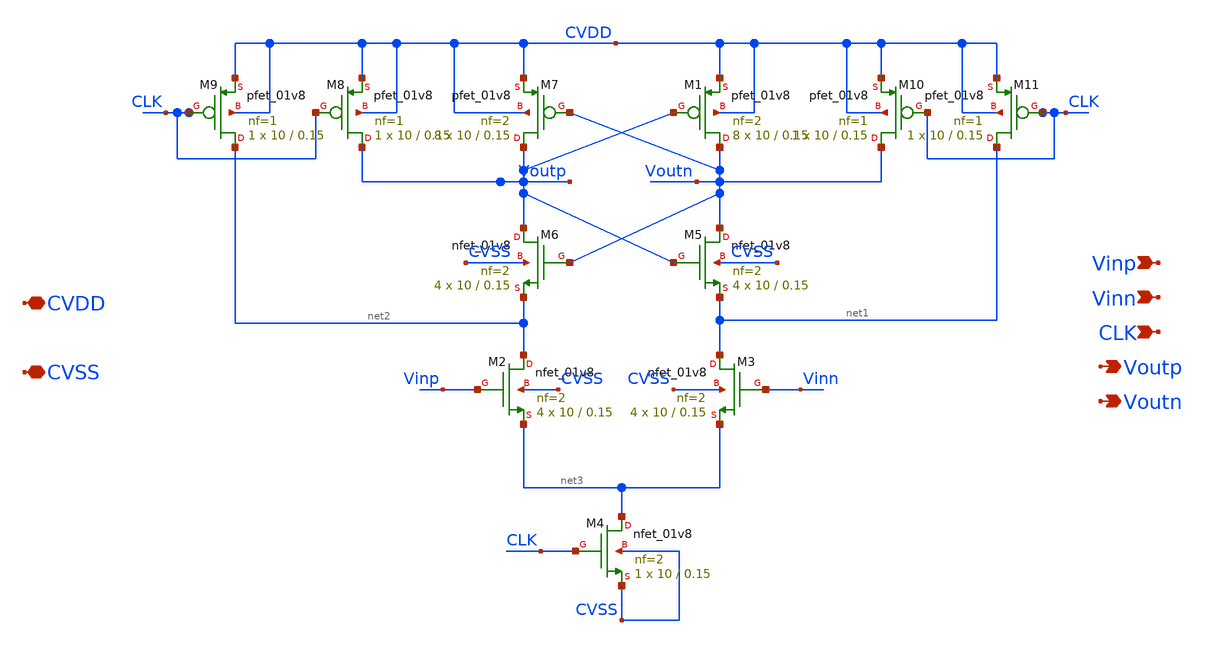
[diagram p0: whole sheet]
** sch_path: xschem/Comparator.sch
**.subckt Comparator CVDD CVSS Vinp Vinn CLK Voutp Voutn
*.iopin CVDD
*.iopin CVSS
*.ipin Vinp
*.ipin Vinn
*.ipin CLK
*.opin Voutp
*.opin Voutn
XM1 Voutn Voutp CVDD CVDD sky130_fd_pr__pfet_01v8 L=0.15 W=10 nf=2 ad='int((nf+1)/2) * W/nf * 0.29' as='int((nf+2)/2) * W/nf * 0.29'
+ pd='2*int((nf+1)/2) * (W/nf + 0.29)' ps='2*int((nf+2)/2) * (W/nf + 0.29)' nrd='0.29 / W' nrs='0.29 / W'
+ sa=0 sb=0 sd=0 mult=8 m=8
XM2 net2 Vinp net3 CVSS sky130_fd_pr__nfet_01v8 L=0.15 W=10 nf=2 ad='int((nf+1)/2) * W/nf * 0.29' as='int((nf+2)/2) * W/nf * 0.29'
+ pd='2*int((nf+1)/2) * (W/nf + 0.29)' ps='2*int((nf+2)/2) * (W/nf + 0.29)' nrd='0.29 / W' nrs='0.29 / W'
+ sa=0 sb=0 sd=0 mult=4 m=4
XM3 net1 Vinn net3 CVSS sky130_fd_pr__nfet_01v8 L=0.15 W=10 nf=2 ad='int((nf+1)/2) * W/nf * 0.29' as='int((nf+2)/2) * W/nf * 0.29'
+ pd='2*int((nf+1)/2) * (W/nf + 0.29)' ps='2*int((nf+2)/2) * (W/nf + 0.29)' nrd='0.29 / W' nrs='0.29 / W'
+ sa=0 sb=0 sd=0 mult=4 m=4
XM4 net3 CLK CVSS CVSS sky130_fd_pr__nfet_01v8 L=0.15 W=10 nf=2 ad='int((nf+1)/2) * W/nf * 0.29' as='int((nf+2)/2) * W/nf * 0.29'
+ pd='2*int((nf+1)/2) * (W/nf + 0.29)' ps='2*int((nf+2)/2) * (W/nf + 0.29)' nrd='0.29 / W' nrs='0.29 / W'
+ sa=0 sb=0 sd=0 mult=1 m=1
XM5 Voutn Voutp net1 CVSS sky130_fd_pr__nfet_01v8 L=0.15 W=10 nf=2 ad='int((nf+1)/2) * W/nf * 0.29' as='int((nf+2)/2) * W/nf * 0.29'
+ pd='2*int((nf+1)/2) * (W/nf + 0.29)' ps='2*int((nf+2)/2) * (W/nf + 0.29)' nrd='0.29 / W' nrs='0.29 / W'
+ sa=0 sb=0 sd=0 mult=4 m=4
XM6 Voutp Voutn net2 CVSS sky130_fd_pr__nfet_01v8 L=0.15 W=10 nf=2 ad='int((nf+1)/2) * W/nf * 0.29' as='int((nf+2)/2) * W/nf * 0.29'
+ pd='2*int((nf+1)/2) * (W/nf + 0.29)' ps='2*int((nf+2)/2) * (W/nf + 0.29)' nrd='0.29 / W' nrs='0.29 / W'
+ sa=0 sb=0 sd=0 mult=4 m=4
XM7 Voutp Voutn CVDD CVDD sky130_fd_pr__pfet_01v8 L=0.15 W=10 nf=2 ad='int((nf+1)/2) * W/nf * 0.29' as='int((nf+2)/2) * W/nf * 0.29'
+ pd='2*int((nf+1)/2) * (W/nf + 0.29)' ps='2*int((nf+2)/2) * (W/nf + 0.29)' nrd='0.29 / W' nrs='0.29 / W'
+ sa=0 sb=0 sd=0 mult=8 m=8
XM8 Voutp CLK CVDD CVDD sky130_fd_pr__pfet_01v8 L=0.15 W=10 nf=1 ad='int((nf+1)/2) * W/nf * 0.29' as='int((nf+2)/2) * W/nf * 0.29'
+ pd='2*int((nf+1)/2) * (W/nf + 0.29)' ps='2*int((nf+2)/2) * (W/nf + 0.29)' nrd='0.29 / W' nrs='0.29 / W'
+ sa=0 sb=0 sd=0 mult=1 m=1
XM9 net2 CLK CVDD CVDD sky130_fd_pr__pfet_01v8 L=0.15 W=10 nf=1 ad='int((nf+1)/2) * W/nf * 0.29' as='int((nf+2)/2) * W/nf * 0.29'
+ pd='2*int((nf+1)/2) * (W/nf + 0.29)' ps='2*int((nf+2)/2) * (W/nf + 0.29)' nrd='0.29 / W' nrs='0.29 / W'
+ sa=0 sb=0 sd=0 mult=1 m=1
XM10 Voutn CLK CVDD CVDD sky130_fd_pr__pfet_01v8 L=0.15 W=10 nf=1 ad='int((nf+1)/2) * W/nf * 0.29' as='int((nf+2)/2) * W/nf * 0.29'
+ pd='2*int((nf+1)/2) * (W/nf + 0.29)' ps='2*int((nf+2)/2) * (W/nf + 0.29)' nrd='0.29 / W' nrs='0.29 / W'
+ sa=0 sb=0 sd=0 mult=1 m=1
XM11 net1 CLK CVDD CVDD sky130_fd_pr__pfet_01v8 L=0.15 W=10 nf=1 ad='int((nf+1)/2) * W/nf * 0.29' as='int((nf+2)/2) * W/nf * 0.29'
+ pd='2*int((nf+1)/2) * (W/nf + 0.29)' ps='2*int((nf+2)/2) * (W/nf + 0.29)' nrd='0.29 / W' nrs='0.29 / W'
+ sa=0 sb=0 sd=0 mult=1 m=1
**.ends
.end
